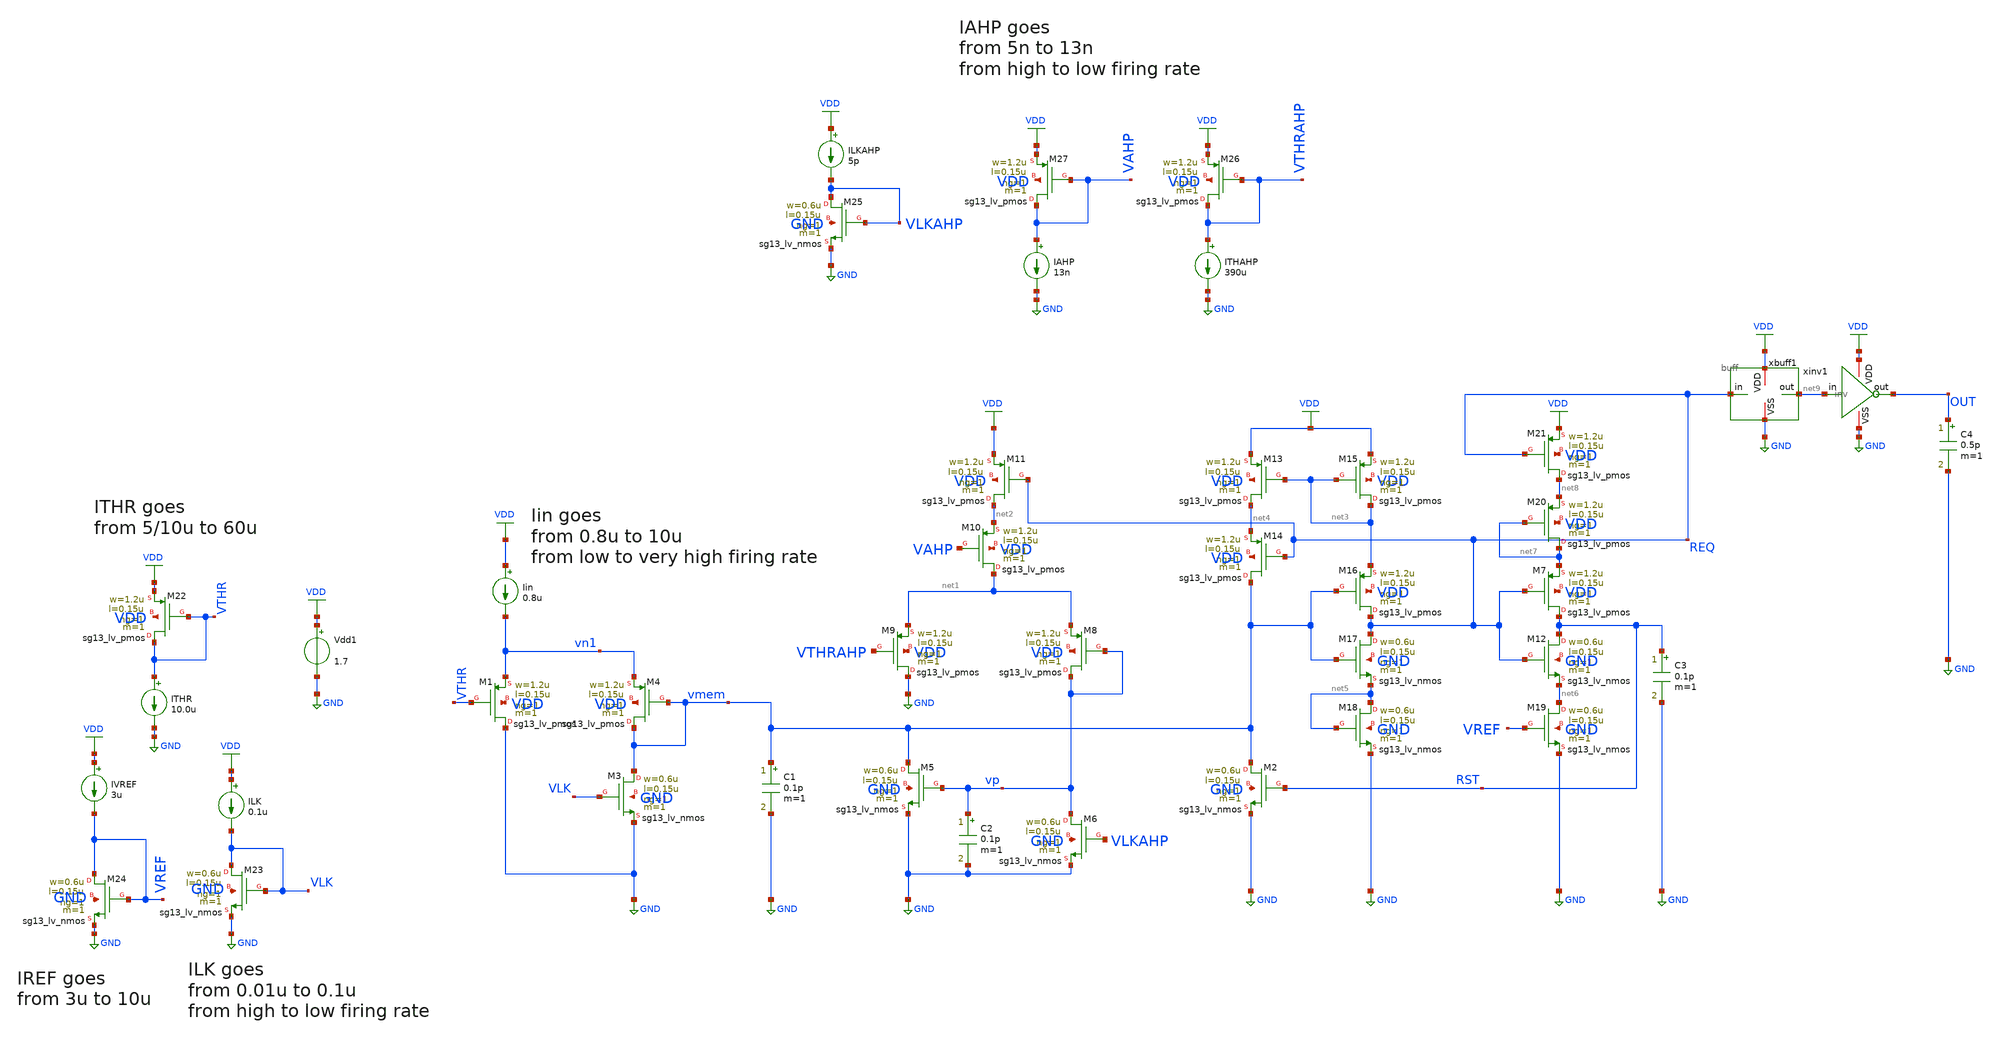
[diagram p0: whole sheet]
** sch_path: blocks/composite/dpi_adexp_neuron/design_data/xschem/neuron_second_working_best.sch
**.subckt neuron_second_working_best
Iin VDD vn1 0.8u
XM3 vmem VLK GND GND sg13_lv_nmos w=0.6u l=0.15u ng=1 m=1 mm_ok=1
XM1 GND VTHR vn1 VDD sg13_lv_pmos w=1.2u l=0.15u ng=1 m=1 mm_ok=1
XM4 vmem vmem vn1 VDD sg13_lv_pmos w=1.2u l=0.15u ng=1 m=1 mm_ok=1
C1 vmem GND 0.1p m=1
XM2 vmem RST GND GND sg13_lv_nmos w=0.6u l=0.15u ng=1 m=1 mm_ok=1
XM5 vmem vp GND GND sg13_lv_nmos w=0.6u l=0.15u ng=1 m=1 mm_ok=1
C2 vp GND 0.1p m=1
XM6 vp VLKAHP GND GND sg13_lv_nmos w=0.6u l=0.15u ng=1 m=1 mm_ok=1
XM8 vp vp net1 VDD sg13_lv_pmos w=1.2u l=0.15u ng=1 m=1 mm_ok=1
XM9 GND VTHRAHP net1 VDD sg13_lv_pmos w=1.2u l=0.15u ng=1 m=1 mm_ok=1
XM10 net1 VAHP net2 VDD sg13_lv_pmos w=1.2u l=0.15u ng=1 m=1 mm_ok=1
XM11 net2 REQ VDD VDD sg13_lv_pmos w=1.2u l=0.15u ng=1 m=1 mm_ok=1
XM13 net4 net3 VDD VDD sg13_lv_pmos w=1.2u l=0.15u ng=1 m=1 mm_ok=1
XM14 vmem REQ net4 VDD sg13_lv_pmos w=1.2u l=0.15u ng=1 m=1 mm_ok=1
XM15 net3 net3 VDD VDD sg13_lv_pmos w=1.2u l=0.15u ng=1 m=1 mm_ok=1
XM16 REQ vmem net3 VDD sg13_lv_pmos w=1.2u l=0.15u ng=1 m=1 mm_ok=1
XM17 REQ vmem net5 GND sg13_lv_nmos w=0.6u l=0.15u ng=1 m=1 mm_ok=1
XM18 net5 net5 GND GND sg13_lv_nmos w=0.6u l=0.15u ng=1 m=1 mm_ok=1
XM7 RST REQ net7 VDD sg13_lv_pmos w=1.2u l=0.15u ng=1 m=1 mm_ok=1
XM12 RST REQ net6 GND sg13_lv_nmos w=0.6u l=0.15u ng=1 m=1 mm_ok=1
XM19 net6 VREF GND GND sg13_lv_nmos w=0.6u l=0.15u ng=1 m=1 mm_ok=1
C3 RST GND 0.1p m=1
XM20 net7 net7 net8 VDD sg13_lv_pmos w=1.2u l=0.15u ng=1 m=1 mm_ok=1
XM21 net8 REQ VDD VDD sg13_lv_pmos w=1.2u l=0.15u ng=1 m=1 mm_ok=1
xbuff1 VDD REQ net9 GND buff
C4 OUT GND 0.5p m=1
xinv1 VDD net9 OUT GND inv
Vdd1 VDD GND 1.7
XM23 VLK VLK GND GND sg13_lv_nmos w=0.6u l=0.15u ng=1 m=1 mm_ok=1
ILK VDD VLK 0.1u
XM24 VREF VREF GND GND sg13_lv_nmos w=0.6u l=0.15u ng=1 m=1 mm_ok=1
IVREF VDD VREF 3u
XM25 VLKAHP VLKAHP GND GND sg13_lv_nmos w=0.6u l=0.15u ng=1 m=1 mm_ok=1
ILKAHP VDD VLKAHP 5p
XM26 VTHRAHP VTHRAHP VDD VDD sg13_lv_pmos w=1.2u l=0.15u ng=1 m=1 mm_ok=1
ITHAHP VTHRAHP GND 390u
XM27 VAHP VAHP VDD VDD sg13_lv_pmos w=1.2u l=0.15u ng=1 m=1 mm_ok=1
IAHP VAHP GND 13n
XM22 VTHR VTHR VDD VDD sg13_lv_pmos w=1.2u l=0.15u ng=1 m=1 mm_ok=1
ITHR VTHR GND 10.0u
**** begin user architecture code

.include diodes.lib
.include sg13g2_bondpad.lib



.options savecurrents
.include neuron_buff_test.save
.param temp=27
.control
set wr_singlescale
set noaskquit
*set appendwrite
set hcopypscolor=1

*Save node voltages and device currents if desired
save all

*Baseline operating point at current deck values
op
write tran_neuron.raw

*alter Vdd1 dc 1.7
*alter Vthr dc 0.9
*alter Vlk dc 0.3
*alter vahp1 dc 1.0
tran 1n 5u
write tran_neuron.raw
*Example plots (uncomment inside ngspice if you want autoplots)
*plot vmem vn1 Vthr Vlk
*plot vmem out
quit
.endc





.lib cornerMOSlv.lib mos_tt
.lib cornerMOShv.lib mos_tt
.lib cornerHBT.lib hbt_typ
.lib cornerRES.lib res_typ



**** end user architecture code
**.ends
.GLOBAL GND
.GLOBAL VDD
.end
